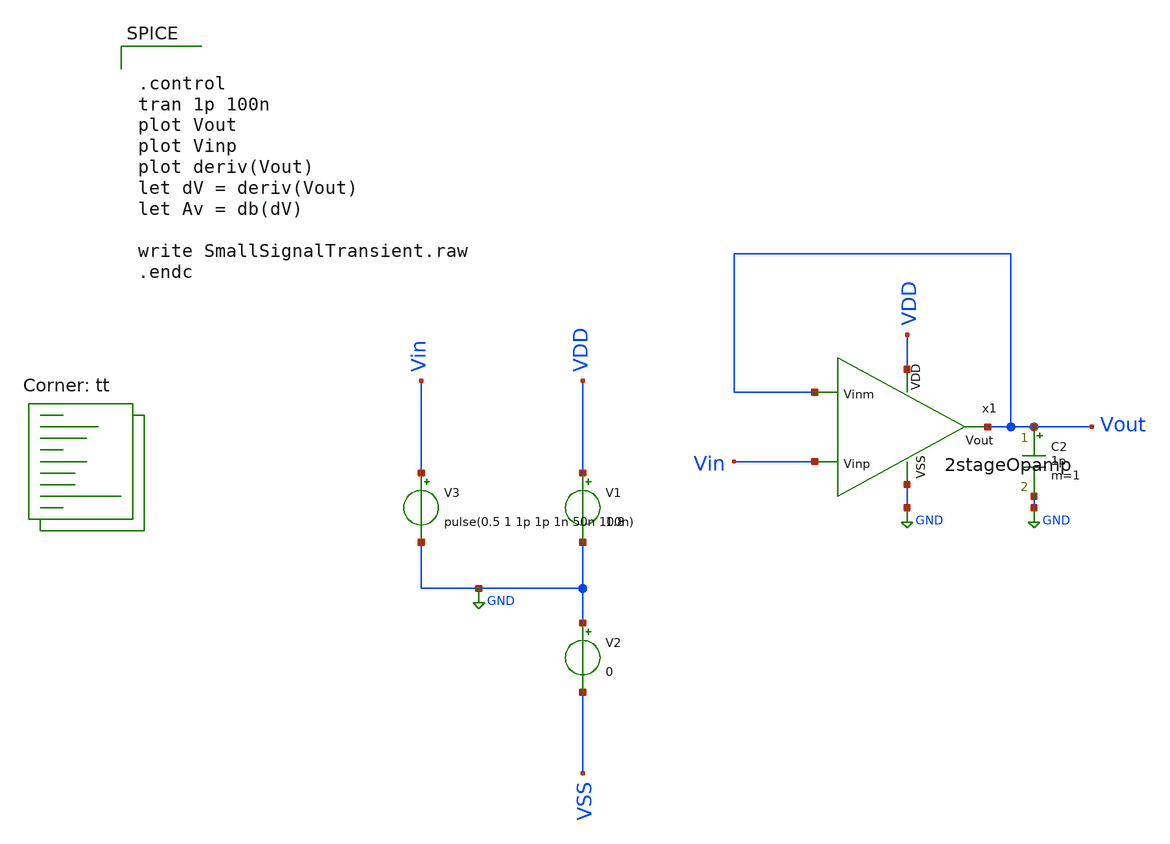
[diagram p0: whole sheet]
** sch_path: xschem/TestBenches/SmallSignalTransient.sch
**.subckt SmallSignalTransient
C2 Vout GND 1p m=1
x1 VDD Vout Vin Vout GND 2stageOpamp
V1 VDD GND 1.8
V2 GND VSS 0
V3 Vin GND pulse(0.5 1 1p 1p 1n 50n 100n)
**** begin user architecture code


.control
tran 1p 100n
plot Vout
plot Vinp
plot deriv(Vout)
let dV = deriv(Vout)
let Av = db(dV)

write SmallSignalTransient.raw
.endc



.lib $::SKYWATER_MODELS/sky130.lib.spice tt
**** end user architecture code
**.ends
.GLOBAL GND
.end
